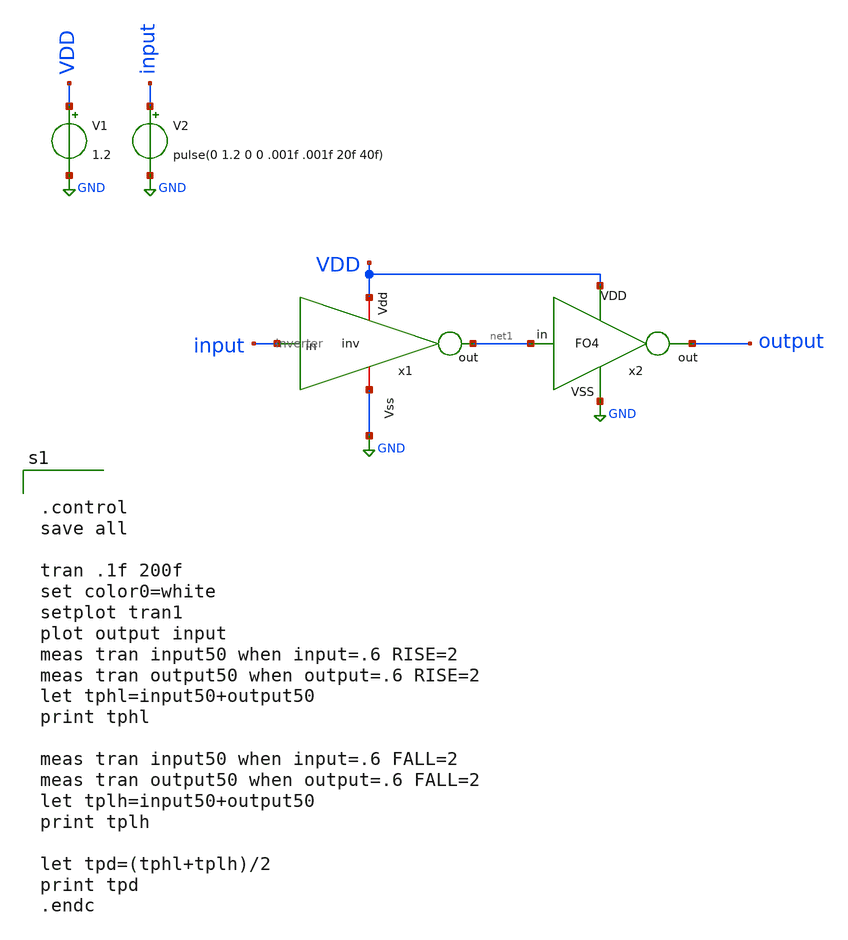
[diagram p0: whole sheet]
** sch_path: inv/inverter_tb.sch
**.subckt inverter_tb
V1 VDD GND 1.2
V2 input GND pulse(0 1.2 0 0 .001f .001f 20f 40f)
x1 input VDD GND net1 inverter
x2 VDD GND net1 output FO4
**** begin user architecture code


.control
save all

tran .1f 200f
set color0=white
setplot tran1
plot output input
meas tran input50 when input=.6 RISE=2
meas tran output50 when output=.6 RISE=2
let tphl=input50+output50
print tphl

meas tran input50 when input=.6 FALL=2
meas tran output50 when output=.6 FALL=2
let tplh=input50+output50
print tplh

let tpd=(tphl+tplh)/2
print tpd
.endc


** opencircuitdesign pdks install
.lib $::SKYWATER_MODELS/sky130.lib.spice tt


**** end user architecture code
**.ends

* expanding   symbol:  inv/inverter.sym # of pins=4
** sym_path: inv/inverter.sym
** sch_path: inv/inverter.sch
.subckt inverter in Vdd Vss out
*.ipin in
*.iopin Vdd
*.iopin Vss
*.opin out
XM2 out in Vss Vss sky130_fd_pr__nfet_01v8 L=0.15 W=1 nf=1 ad='int((1 + 1)/2) * 1 / 1 * 0.29' as='int((1 + 2)/2) * 1 / 1 * 0.29'
+ pd='2*int((1 + 1)/2) * (1 / 1 + 0.29)' ps='2*int((1 + 2)/2) * (1 / 1 + 0.29)' nrd='0.29 / 1 ' nrs='0.29 / 1 '
+ sa=0 sb=0 sd=0 mult=1 m=1
XM11 out in Vdd Vdd sky130_fd_pr__pfet_01v8 L=0.15 W=1 nf=1 ad='int((nf+1)/2) * W/nf * 0.29' as='int((nf+2)/2) * W/nf * 0.29'
+ pd='2*int((nf+1)/2) * (W/nf + 0.29)' ps='2*int((nf+2)/2) * (W/nf + 0.29)' nrd='0.29 / W' nrs='0.29 / W'
+ sa=0 sb=0 sd=0 mult=1 m=1
.ends


* expanding   symbol:  FO4/FO4.sym # of pins=4
** sym_path: FO4/FO4.sym
** sch_path: FO4/FO4.sch
.subckt FO4 VDD VSS in out
*.ipin VDD
*.ipin VSS
*.ipin in
*.opin out
XM1 net1 in VSS VSS sky130_fd_pr__nfet_01v8 L=0.15 W=0.7 nf=1 ad='int((nf+1)/2) * W/nf * 0.29' as='int((nf+2)/2) * W/nf * 0.29'
+ pd='2*int((nf+1)/2) * (W/nf + 0.29)' ps='2*int((nf+2)/2) * (W/nf + 0.29)' nrd='0.29 / W' nrs='0.29 / W'
+ sa=0 sb=0 sd=0 mult=1 m=1
XM2 net1 in VDD VDD sky130_fd_pr__pfet_01v8 L=0.15 W=1 nf=1 ad='int((nf+1)/2) * W/nf * 0.29' as='int((nf+2)/2) * W/nf * 0.29'
+ pd='2*int((nf+1)/2) * (W/nf + 0.29)' ps='2*int((nf+2)/2) * (W/nf + 0.29)' nrd='0.29 / W' nrs='0.29 / W'
+ sa=0 sb=0 sd=0 mult=1 m=1
XM3 net2 in VSS VSS sky130_fd_pr__nfet_01v8 L=0.15 W=0.7 nf=1 ad='int((nf+1)/2) * W/nf * 0.29' as='int((nf+2)/2) * W/nf * 0.29'
+ pd='2*int((nf+1)/2) * (W/nf + 0.29)' ps='2*int((nf+2)/2) * (W/nf + 0.29)' nrd='0.29 / W' nrs='0.29 / W'
+ sa=0 sb=0 sd=0 mult=1 m=1
XM4 net2 in VDD VDD sky130_fd_pr__pfet_01v8 L=0.15 W=1 nf=1 ad='int((nf+1)/2) * W/nf * 0.29' as='int((nf+2)/2) * W/nf * 0.29'
+ pd='2*int((nf+1)/2) * (W/nf + 0.29)' ps='2*int((nf+2)/2) * (W/nf + 0.29)' nrd='0.29 / W' nrs='0.29 / W'
+ sa=0 sb=0 sd=0 mult=1 m=1
XM5 net3 in VSS VSS sky130_fd_pr__nfet_01v8 L=0.15 W=0.7 nf=1 ad='int((nf+1)/2) * W/nf * 0.29' as='int((nf+2)/2) * W/nf * 0.29'
+ pd='2*int((nf+1)/2) * (W/nf + 0.29)' ps='2*int((nf+2)/2) * (W/nf + 0.29)' nrd='0.29 / W' nrs='0.29 / W'
+ sa=0 sb=0 sd=0 mult=1 m=1
XM6 net3 in VDD VDD sky130_fd_pr__pfet_01v8 L=0.15 W=1 nf=1 ad='int((nf+1)/2) * W/nf * 0.29' as='int((nf+2)/2) * W/nf * 0.29'
+ pd='2*int((nf+1)/2) * (W/nf + 0.29)' ps='2*int((nf+2)/2) * (W/nf + 0.29)' nrd='0.29 / W' nrs='0.29 / W'
+ sa=0 sb=0 sd=0 mult=1 m=1
XM7 out in VSS VSS sky130_fd_pr__nfet_01v8 L=0.15 W=0.7 nf=1 ad='int((nf+1)/2) * W/nf * 0.29' as='int((nf+2)/2) * W/nf * 0.29'
+ pd='2*int((nf+1)/2) * (W/nf + 0.29)' ps='2*int((nf+2)/2) * (W/nf + 0.29)' nrd='0.29 / W' nrs='0.29 / W'
+ sa=0 sb=0 sd=0 mult=1 m=1
XM8 out in VDD VDD sky130_fd_pr__pfet_01v8 L=0.15 W=1 nf=1 ad='int((nf+1)/2) * W/nf * 0.29' as='int((nf+2)/2) * W/nf * 0.29'
+ pd='2*int((nf+1)/2) * (W/nf + 0.29)' ps='2*int((nf+2)/2) * (W/nf + 0.29)' nrd='0.29 / W' nrs='0.29 / W'
+ sa=0 sb=0 sd=0 mult=1 m=1
.ends

.GLOBAL GND
.end
